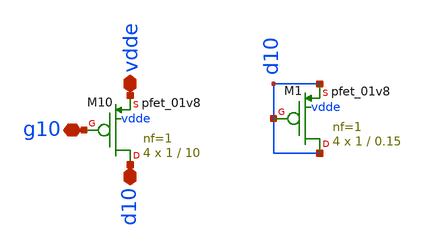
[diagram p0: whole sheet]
** sch_path: magic/secondstage.sch
**.subckt secondstage vdde g10 d10
*.iopin vdde
*.iopin g10
*.iopin d10
XM10 d10 g10 vdde vdde sky130_fd_pr__pfet_01v8 L=10 W=1 nf=1 ad='int((nf+1)/2) * W/nf * 0.29' as='int((nf+2)/2) * W/nf * 0.29'
+ pd='2*int((nf+1)/2) * (W/nf + 0.29)' ps='2*int((nf+2)/2) * (W/nf + 0.29)' nrd='0.29 / W' nrs='0.29 / W'
+ sa=0 sb=0 sd=0 mult=4 m=4
XM1 d10 d10 d10 vdde sky130_fd_pr__pfet_01v8 L=0.15 W=1 nf=1 ad='int((nf+1)/2) * W/nf * 0.29' as='int((nf+2)/2) * W/nf * 0.29'
+ pd='2*int((nf+1)/2) * (W/nf + 0.29)' ps='2*int((nf+2)/2) * (W/nf + 0.29)' nrd='0.29 / W' nrs='0.29 / W'
+ sa=0 sb=0 sd=0 mult=4 m=4
**.ends
.end
